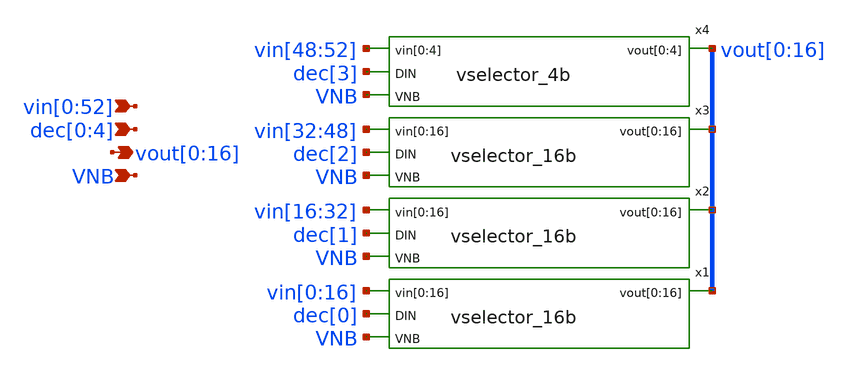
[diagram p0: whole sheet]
** sch_path: xschem/vselector_6b_2v_stage_1.sch
**.subckt vselector_6b_2v_stage_1
*+ vin[0],vin[1],vin[2],vin[3],vin[4],vin[5],vin[6],vin[7],vin[8],vin[9],vin[10],vin[11],vin[12],vin[13],vin[14],vin[15],vin[16],vin[17],vin[18],vin[19],vin[20],vin[21],vin[22],vin[23],vin[24],vin[25],vin[26],vin[27],vin[28],vin[29],vin[30],vin[31],vin[32],vin[33],vin[34],vin[35],vin[36],vin[37],vin[38],vin[39],vin[40],vin[41],vin[42],vin[43],vin[44],vin[45],vin[46],vin[47],vin[48],vin[49],vin[50],vin[51],vin[52]
*+ vout[0],vout[1],vout[2],vout[3],vout[4],vout[5],vout[6],vout[7],vout[8],vout[9],vout[10],vout[11],vout[12],vout[13],vout[14],vout[15],vout[16] VNB dec[0],dec[1],dec[2],dec[3],dec[4]
*.ipin
*+ vin[0],vin[1],vin[2],vin[3],vin[4],vin[5],vin[6],vin[7],vin[8],vin[9],vin[10],vin[11],vin[12],vin[13],vin[14],vin[15],vin[16],vin[17],vin[18],vin[19],vin[20],vin[21],vin[22],vin[23],vin[24],vin[25],vin[26],vin[27],vin[28],vin[29],vin[30],vin[31],vin[32],vin[33],vin[34],vin[35],vin[36],vin[37],vin[38],vin[39],vin[40],vin[41],vin[42],vin[43],vin[44],vin[45],vin[46],vin[47],vin[48],vin[49],vin[50],vin[51],vin[52]
*.opin
*+ vout[0],vout[1],vout[2],vout[3],vout[4],vout[5],vout[6],vout[7],vout[8],vout[9],vout[10],vout[11],vout[12],vout[13],vout[14],vout[15],vout[16]
*.ipin VNB
*.ipin dec[0],dec[1],dec[2],dec[3],dec[4]
x1 vin[0] vin[1] vin[2] vin[3] vin[4] vin[5] vin[6] vin[7] vin[8] vin[9] vin[10] vin[11] vin[12]
+ vin[13] vin[14] vin[15] vin[16] dec[0] vout[0] vout[1] vout[2] vout[3] vout[4] vout[5] vout[6] vout[7]
+ vout[8] vout[9] vout[10] vout[11] vout[12] vout[13] vout[14] vout[15] vout[16] VNB vselector_16b
x2 vin[16] vin[17] vin[18] vin[19] vin[20] vin[21] vin[22] vin[23] vin[24] vin[25] vin[26] vin[27]
+ vin[28] vin[29] vin[30] vin[31] vin[32] dec[1] vout[0] vout[1] vout[2] vout[3] vout[4] vout[5] vout[6]
+ vout[7] vout[8] vout[9] vout[10] vout[11] vout[12] vout[13] vout[14] vout[15] vout[16] VNB vselector_16b
x3 vin[32] vin[33] vin[34] vin[35] vin[36] vin[37] vin[38] vin[39] vin[40] vin[41] vin[42] vin[43]
+ vin[44] vin[45] vin[46] vin[47] vin[48] dec[2] vout[0] vout[1] vout[2] vout[3] vout[4] vout[5] vout[6]
+ vout[7] vout[8] vout[9] vout[10] vout[11] vout[12] vout[13] vout[14] vout[15] vout[16] VNB vselector_16b
x4 vin[48] vin[49] vin[50] vin[51] vin[52] dec[3] vout[0] vout[1] vout[2] vout[3] vout[4] VNB
+ vselector_4b
**.ends

* expanding   symbol:  vselector_16b.sym # of pins=4
** sym_path: xschem/vselector_16b.sym
** sch_path: xschem/vselector_16b.sch
.subckt vselector_16b vin[0] vin[1] vin[2] vin[3] vin[4] vin[5] vin[6] vin[7] vin[8] vin[9] vin[10]
+ vin[11] vin[12] vin[13] vin[14] vin[15] vin[16] DIN vout[0] vout[1] vout[2] vout[3] vout[4] vout[5] vout[6]
+ vout[7] vout[8] vout[9] vout[10] vout[11] vout[12] vout[13] vout[14] vout[15] vout[16] VNB
*.ipin
*+ vin[0],vin[1],vin[2],vin[3],vin[4],vin[5],vin[6],vin[7],vin[8],vin[9],vin[10],vin[11],vin[12],vin[13],vin[14],vin[15],vin[16]
*.opin
*+ vout[0],vout[1],vout[2],vout[3],vout[4],vout[5],vout[6],vout[7],vout[8],vout[9],vout[10],vout[11],vout[12],vout[13],vout[14],vout[15],vout[16]
*.ipin VNB
*.ipin DIN
.param wp=0.42 wn=0.42 l=0.5

XM1 vout[0] DIN vin[0] net1 sky130_fd_pr__nfet_g5v0d10v5 L=l W=wn nf=1 ad='int((nf+1)/2) * W/nf * 0.29'
+ as='int((nf+2)/2) * W/nf * 0.29' pd='2*int((nf+1)/2) * (W/nf + 0.29)' ps='2*int((nf+2)/2) * (W/nf + 0.29)'
+ nrd='0.29 / W' nrs='0.29 / W' sa=0 sb=0 sd=0 mult=1 m=1
XM2 vout[1] DIN vin[1] net1 sky130_fd_pr__nfet_g5v0d10v5 L=l W=wn nf=1 ad='int((nf+1)/2) * W/nf * 0.29'
+ as='int((nf+2)/2) * W/nf * 0.29' pd='2*int((nf+1)/2) * (W/nf + 0.29)' ps='2*int((nf+2)/2) * (W/nf + 0.29)'
+ nrd='0.29 / W' nrs='0.29 / W' sa=0 sb=0 sd=0 mult=1 m=1
XM3 vout[2] DIN vin[2] net1 sky130_fd_pr__nfet_g5v0d10v5 L=l W=wn nf=1 ad='int((nf+1)/2) * W/nf * 0.29'
+ as='int((nf+2)/2) * W/nf * 0.29' pd='2*int((nf+1)/2) * (W/nf + 0.29)' ps='2*int((nf+2)/2) * (W/nf + 0.29)'
+ nrd='0.29 / W' nrs='0.29 / W' sa=0 sb=0 sd=0 mult=1 m=1
XM4 vout[3] DIN vin[3] net1 sky130_fd_pr__nfet_g5v0d10v5 L=l W=wn nf=1 ad='int((nf+1)/2) * W/nf * 0.29'
+ as='int((nf+2)/2) * W/nf * 0.29' pd='2*int((nf+1)/2) * (W/nf + 0.29)' ps='2*int((nf+2)/2) * (W/nf + 0.29)'
+ nrd='0.29 / W' nrs='0.29 / W' sa=0 sb=0 sd=0 mult=1 m=1
XM5 vout[4] DIN vin[4] net1 sky130_fd_pr__nfet_g5v0d10v5 L=l W=wn nf=1 ad='int((nf+1)/2) * W/nf * 0.29'
+ as='int((nf+2)/2) * W/nf * 0.29' pd='2*int((nf+1)/2) * (W/nf + 0.29)' ps='2*int((nf+2)/2) * (W/nf + 0.29)'
+ nrd='0.29 / W' nrs='0.29 / W' sa=0 sb=0 sd=0 mult=1 m=1
XM6 vout[5] DIN vin[5] net1 sky130_fd_pr__nfet_g5v0d10v5 L=l W=wn nf=1 ad='int((nf+1)/2) * W/nf * 0.29'
+ as='int((nf+2)/2) * W/nf * 0.29' pd='2*int((nf+1)/2) * (W/nf + 0.29)' ps='2*int((nf+2)/2) * (W/nf + 0.29)'
+ nrd='0.29 / W' nrs='0.29 / W' sa=0 sb=0 sd=0 mult=1 m=1
XM7 vout[6] DIN vin[6] net1 sky130_fd_pr__nfet_g5v0d10v5 L=l W=wn nf=1 ad='int((nf+1)/2) * W/nf * 0.29'
+ as='int((nf+2)/2) * W/nf * 0.29' pd='2*int((nf+1)/2) * (W/nf + 0.29)' ps='2*int((nf+2)/2) * (W/nf + 0.29)'
+ nrd='0.29 / W' nrs='0.29 / W' sa=0 sb=0 sd=0 mult=1 m=1
XM8 vout[7] DIN vin[7] net1 sky130_fd_pr__nfet_g5v0d10v5 L=l W=wn nf=1 ad='int((nf+1)/2) * W/nf * 0.29'
+ as='int((nf+2)/2) * W/nf * 0.29' pd='2*int((nf+1)/2) * (W/nf + 0.29)' ps='2*int((nf+2)/2) * (W/nf + 0.29)'
+ nrd='0.29 / W' nrs='0.29 / W' sa=0 sb=0 sd=0 mult=1 m=1
XM9 vout[8] DIN vin[8] net1 sky130_fd_pr__nfet_g5v0d10v5 L=l W=wn nf=1 ad='int((nf+1)/2) * W/nf * 0.29'
+ as='int((nf+2)/2) * W/nf * 0.29' pd='2*int((nf+1)/2) * (W/nf + 0.29)' ps='2*int((nf+2)/2) * (W/nf + 0.29)'
+ nrd='0.29 / W' nrs='0.29 / W' sa=0 sb=0 sd=0 mult=1 m=1
XM10 vout[9] DIN vin[9] net1 sky130_fd_pr__nfet_g5v0d10v5 L=l W=wn nf=1 ad='int((nf+1)/2) * W/nf * 0.29'
+ as='int((nf+2)/2) * W/nf * 0.29' pd='2*int((nf+1)/2) * (W/nf + 0.29)' ps='2*int((nf+2)/2) * (W/nf + 0.29)'
+ nrd='0.29 / W' nrs='0.29 / W' sa=0 sb=0 sd=0 mult=1 m=1
XM11 vout[10] DIN vin[10] net1 sky130_fd_pr__nfet_g5v0d10v5 L=l W=wn nf=1 ad='int((nf+1)/2) * W/nf * 0.29'
+ as='int((nf+2)/2) * W/nf * 0.29' pd='2*int((nf+1)/2) * (W/nf + 0.29)' ps='2*int((nf+2)/2) * (W/nf + 0.29)'
+ nrd='0.29 / W' nrs='0.29 / W' sa=0 sb=0 sd=0 mult=1 m=1
XM12 vout[11] DIN vin[11] net1 sky130_fd_pr__nfet_g5v0d10v5 L=l W=wn nf=1 ad='int((nf+1)/2) * W/nf * 0.29'
+ as='int((nf+2)/2) * W/nf * 0.29' pd='2*int((nf+1)/2) * (W/nf + 0.29)' ps='2*int((nf+2)/2) * (W/nf + 0.29)'
+ nrd='0.29 / W' nrs='0.29 / W' sa=0 sb=0 sd=0 mult=1 m=1
XM13 vout[12] DIN vin[12] net1 sky130_fd_pr__nfet_g5v0d10v5 L=l W=wn nf=1 ad='int((nf+1)/2) * W/nf * 0.29'
+ as='int((nf+2)/2) * W/nf * 0.29' pd='2*int((nf+1)/2) * (W/nf + 0.29)' ps='2*int((nf+2)/2) * (W/nf + 0.29)'
+ nrd='0.29 / W' nrs='0.29 / W' sa=0 sb=0 sd=0 mult=1 m=1
XM14 vout[13] DIN vin[13] net1 sky130_fd_pr__nfet_g5v0d10v5 L=l W=wn nf=1 ad='int((nf+1)/2) * W/nf * 0.29'
+ as='int((nf+2)/2) * W/nf * 0.29' pd='2*int((nf+1)/2) * (W/nf + 0.29)' ps='2*int((nf+2)/2) * (W/nf + 0.29)'
+ nrd='0.29 / W' nrs='0.29 / W' sa=0 sb=0 sd=0 mult=1 m=1
XM15 vout[14] DIN vin[14] net1 sky130_fd_pr__nfet_g5v0d10v5 L=l W=wn nf=1 ad='int((nf+1)/2) * W/nf * 0.29'
+ as='int((nf+2)/2) * W/nf * 0.29' pd='2*int((nf+1)/2) * (W/nf + 0.29)' ps='2*int((nf+2)/2) * (W/nf + 0.29)'
+ nrd='0.29 / W' nrs='0.29 / W' sa=0 sb=0 sd=0 mult=1 m=1
XM16 vout[15] DIN vin[15] net1 sky130_fd_pr__nfet_g5v0d10v5 L=l W=wn nf=1 ad='int((nf+1)/2) * W/nf * 0.29'
+ as='int((nf+2)/2) * W/nf * 0.29' pd='2*int((nf+1)/2) * (W/nf + 0.29)' ps='2*int((nf+2)/2) * (W/nf + 0.29)'
+ nrd='0.29 / W' nrs='0.29 / W' sa=0 sb=0 sd=0 mult=1 m=1
XM17 vout[16] DIN vin[16] net1 sky130_fd_pr__nfet_g5v0d10v5 L=l W=wn nf=1 ad='int((nf+1)/2) * W/nf * 0.29'
+ as='int((nf+2)/2) * W/nf * 0.29' pd='2*int((nf+1)/2) * (W/nf + 0.29)' ps='2*int((nf+2)/2) * (W/nf + 0.29)'
+ nrd='0.29 / W' nrs='0.29 / W' sa=0 sb=0 sd=0 mult=1 m=1
.ends


* expanding   symbol:  vselector_4b.sym # of pins=4
** sym_path: xschem/vselector_4b.sym
** sch_path: xschem/vselector_4b.sch
.subckt vselector_4b vin[0] vin[1] vin[2] vin[3] vin[4] DIN vout[0] vout[1] vout[2] vout[3] vout[4]
+ VNB
*.ipin vin[0],vin[1],vin[2],vin[3],vin[4]
*.opin vout[0],vout[1],vout[2],vout[3],vout[4]
*.ipin VNB
*.ipin DIN
.param wp=0.42 wn=0.42 l=0.5

XM1 vout[0] DIN vin[0] VNB sky130_fd_pr__nfet_g5v0d10v5 L=l W=wn nf=1 ad='int((nf+1)/2) * W/nf * 0.29'
+ as='int((nf+2)/2) * W/nf * 0.29' pd='2*int((nf+1)/2) * (W/nf + 0.29)' ps='2*int((nf+2)/2) * (W/nf + 0.29)'
+ nrd='0.29 / W' nrs='0.29 / W' sa=0 sb=0 sd=0 mult=1 m=1
XM2 vout[1] DIN vin[1] VNB sky130_fd_pr__nfet_g5v0d10v5 L=l W=wn nf=1 ad='int((nf+1)/2) * W/nf * 0.29'
+ as='int((nf+2)/2) * W/nf * 0.29' pd='2*int((nf+1)/2) * (W/nf + 0.29)' ps='2*int((nf+2)/2) * (W/nf + 0.29)'
+ nrd='0.29 / W' nrs='0.29 / W' sa=0 sb=0 sd=0 mult=1 m=1
XM3 vout[2] DIN vin[2] VNB sky130_fd_pr__nfet_g5v0d10v5 L=l W=wn nf=1 ad='int((nf+1)/2) * W/nf * 0.29'
+ as='int((nf+2)/2) * W/nf * 0.29' pd='2*int((nf+1)/2) * (W/nf + 0.29)' ps='2*int((nf+2)/2) * (W/nf + 0.29)'
+ nrd='0.29 / W' nrs='0.29 / W' sa=0 sb=0 sd=0 mult=1 m=1
XM4 vout[3] DIN vin[3] VNB sky130_fd_pr__nfet_g5v0d10v5 L=l W=wn nf=1 ad='int((nf+1)/2) * W/nf * 0.29'
+ as='int((nf+2)/2) * W/nf * 0.29' pd='2*int((nf+1)/2) * (W/nf + 0.29)' ps='2*int((nf+2)/2) * (W/nf + 0.29)'
+ nrd='0.29 / W' nrs='0.29 / W' sa=0 sb=0 sd=0 mult=1 m=1
XM5 vout[4] DIN vin[4] VNB sky130_fd_pr__nfet_g5v0d10v5 L=l W=wn nf=1 ad='int((nf+1)/2) * W/nf * 0.29'
+ as='int((nf+2)/2) * W/nf * 0.29' pd='2*int((nf+1)/2) * (W/nf + 0.29)' ps='2*int((nf+2)/2) * (W/nf + 0.29)'
+ nrd='0.29 / W' nrs='0.29 / W' sa=0 sb=0 sd=0 mult=1 m=1
.ends

.end
